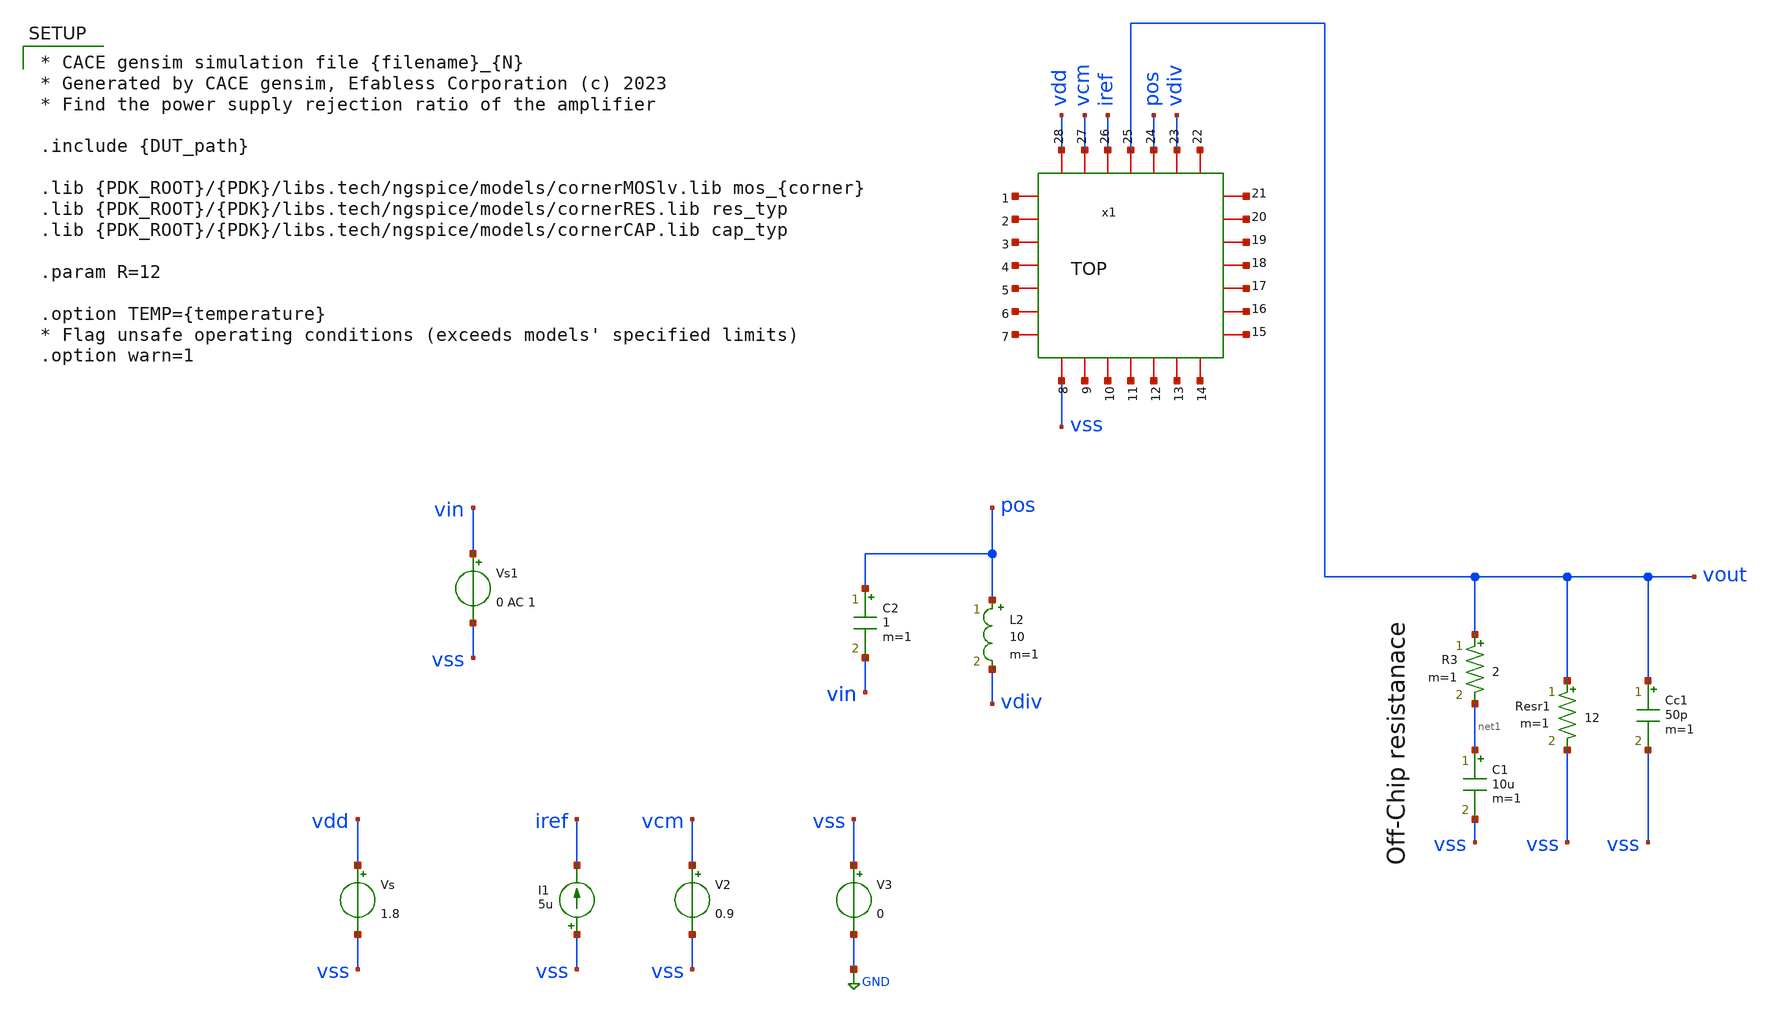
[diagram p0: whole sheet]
** sch_path: AC3E-IHP_ALDO/val/cace/TOP_ldo_cl_openloop.sch
**.subckt TOP_ldo_cl_openloop
C2 pos vin 1 m=1
L2 pos vdiv 10 m=1
C1 net1 vss 10u m=1
R3 vout net1 2 m=1
Resr1 vout vss 12 m=1
Cc1 vout vss 50p m=1
V2 vcm vss 0.9
V3 vss GND 0
I1 vss iref 5u
Vs vdd vss 1.8
Vs1 vin vss 0 AC 1
x1 vdd net2 vdiv pos iref vcm vout net3 net4 net5 net6 net7 net8 net9 net10 net11 net12 net13 net14
+ net15 net16 vss net17 net18 net19 net20 net21 net22 TOP
**** begin user architecture code



*Simulation
.control
pre_osdi /home/ac3e/Documents/psp103_nqs.osdi

ac dec 100 1 10G
setplot ac1
meas ac GBW when vdb(vout)=0
meas ac DCG find vdb(vout) at=1
let Openloop_Gain = DCG
meas ac PM find vp(vout) when vdb(vout)=0
let Phase_Margin = PM*180/PI

meas ac GM find vdb(vout) when vp(vout)=0

wrdata {simpath}/{filename}_{N}.data Openloop_Gain
wrdata {simpath}/{filename}_{N}.data Phase_Margin
quit
.endc

.end



* CACE gensim simulation file {filename}_{N}
* Generated by CACE gensim, Efabless Corporation (c) 2023
* Find the power supply rejection ratio of the amplifier

.include {DUT_path}

.lib {PDK_ROOT}/{PDK}/libs.tech/ngspice/models/cornerMOSlv.lib mos_{corner}
.lib {PDK_ROOT}/{PDK}/libs.tech/ngspice/models/cornerRES.lib res_typ
.lib {PDK_ROOT}/{PDK}/libs.tech/ngspice/models/cornerCAP.lib cap_typ

.param R=12

.option TEMP={temperature}
* Flag unsafe operating conditions (exceeds models' specified limits)
.option warn=1


**** end user architecture code
**.ends
.GLOBAL GND
.end
